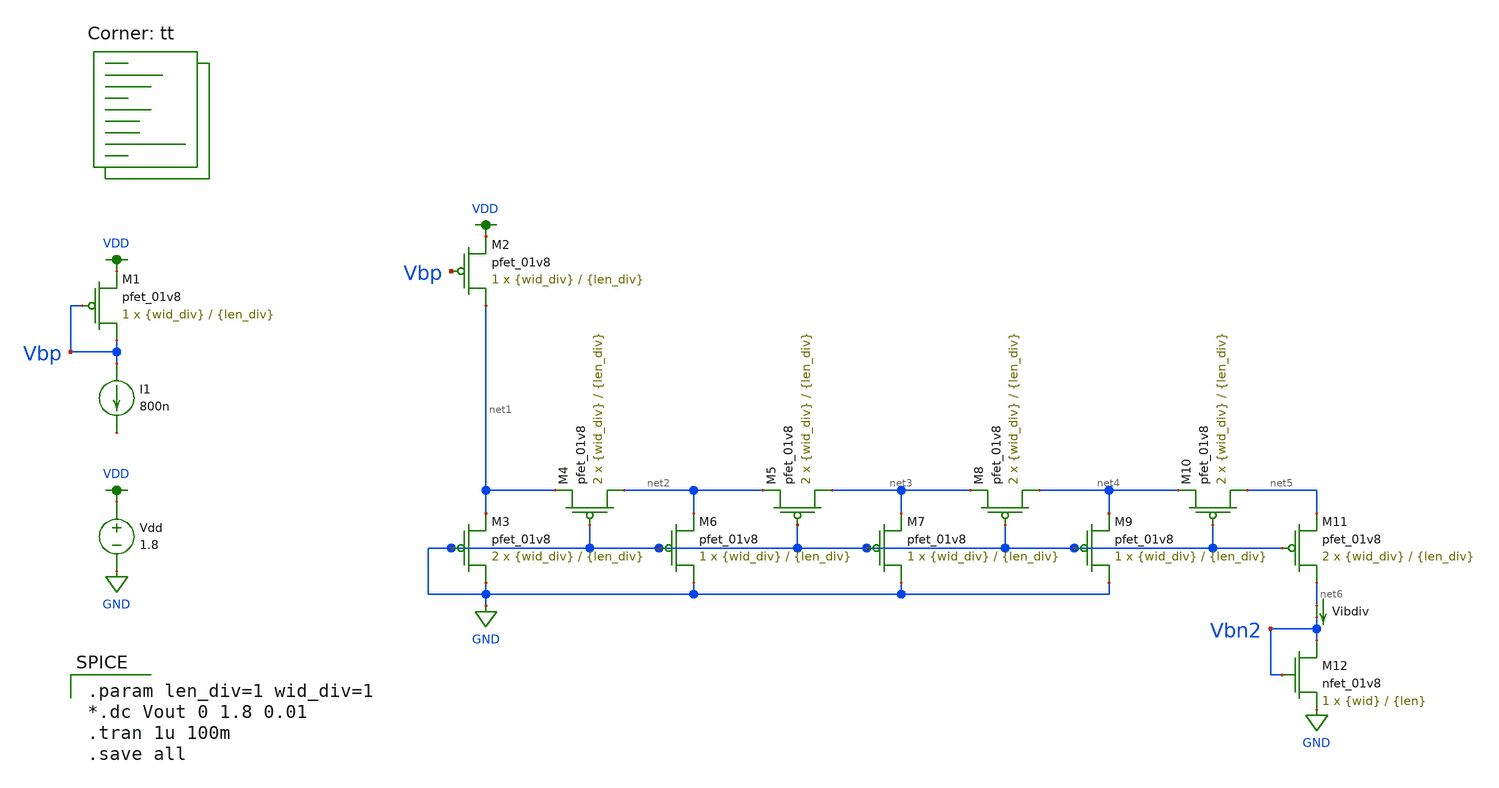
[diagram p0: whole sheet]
** sch_path: mp3/Reference Designs/current_divider_tb.sch
**.subckt current_divider_tb
I1 Vbp net7 800n
Vdd VDD GND 1.8
XM1 Vbp Vbp VDD VDD sky130_fd_pr__pfet_01v8 L={len_div} W={wid_div} nf=1 ad='int((nf+1)/2) * W/nf * 0.29'
+ as='int((nf+2)/2) * W/nf * 0.29' pd='2*int((nf+1)/2) * (W/nf + 0.29)' ps='2*int((nf+2)/2) * (W/nf + 0.29)'
+ nrd='0.29 / W' nrs='0.29 / W' sa=0 sb=0 sd=0 mult=1 m=1
XM2 net1 Vbp VDD VDD sky130_fd_pr__pfet_01v8 L={len_div} W={wid_div} nf=1 ad='int((nf+1)/2) * W/nf * 0.29'
+ as='int((nf+2)/2) * W/nf * 0.29' pd='2*int((nf+1)/2) * (W/nf + 0.29)' ps='2*int((nf+2)/2) * (W/nf + 0.29)'
+ nrd='0.29 / W' nrs='0.29 / W' sa=0 sb=0 sd=0 mult=1 m=1
XM3 GND GND net1 VDD sky130_fd_pr__pfet_01v8 L={len_div} W={wid_div} nf=1 ad='int((nf+1)/2) * W/nf * 0.29'
+ as='int((nf+2)/2) * W/nf * 0.29' pd='2*int((nf+1)/2) * (W/nf + 0.29)' ps='2*int((nf+2)/2) * (W/nf + 0.29)'
+ nrd='0.29 / W' nrs='0.29 / W' sa=0 sb=0 sd=0 mult=2 m=2
XM4 net2 GND net1 VDD sky130_fd_pr__pfet_01v8 L={len_div} W={wid_div} nf=1 ad='int((nf+1)/2) * W/nf * 0.29'
+ as='int((nf+2)/2) * W/nf * 0.29' pd='2*int((nf+1)/2) * (W/nf + 0.29)' ps='2*int((nf+2)/2) * (W/nf + 0.29)'
+ nrd='0.29 / W' nrs='0.29 / W' sa=0 sb=0 sd=0 mult=2 m=2
XM6 GND GND net2 VDD sky130_fd_pr__pfet_01v8 L={len_div} W={wid_div} nf=1 ad='int((nf+1)/2) * W/nf * 0.29'
+ as='int((nf+2)/2) * W/nf * 0.29' pd='2*int((nf+1)/2) * (W/nf + 0.29)' ps='2*int((nf+2)/2) * (W/nf + 0.29)'
+ nrd='0.29 / W' nrs='0.29 / W' sa=0 sb=0 sd=0 mult=1 m=1
XM5 net3 GND net2 VDD sky130_fd_pr__pfet_01v8 L={len_div} W={wid_div} nf=1 ad='int((nf+1)/2) * W/nf * 0.29'
+ as='int((nf+2)/2) * W/nf * 0.29' pd='2*int((nf+1)/2) * (W/nf + 0.29)' ps='2*int((nf+2)/2) * (W/nf + 0.29)'
+ nrd='0.29 / W' nrs='0.29 / W' sa=0 sb=0 sd=0 mult=2 m=2
XM7 GND GND net3 VDD sky130_fd_pr__pfet_01v8 L={len_div} W={wid_div} nf=1 ad='int((nf+1)/2) * W/nf * 0.29'
+ as='int((nf+2)/2) * W/nf * 0.29' pd='2*int((nf+1)/2) * (W/nf + 0.29)' ps='2*int((nf+2)/2) * (W/nf + 0.29)'
+ nrd='0.29 / W' nrs='0.29 / W' sa=0 sb=0 sd=0 mult=1 m=1
XM8 net4 GND net3 VDD sky130_fd_pr__pfet_01v8 L={len_div} W={wid_div} nf=1 ad='int((nf+1)/2) * W/nf * 0.29'
+ as='int((nf+2)/2) * W/nf * 0.29' pd='2*int((nf+1)/2) * (W/nf + 0.29)' ps='2*int((nf+2)/2) * (W/nf + 0.29)'
+ nrd='0.29 / W' nrs='0.29 / W' sa=0 sb=0 sd=0 mult=2 m=2
XM9 GND GND net4 VDD sky130_fd_pr__pfet_01v8 L={len_div} W={wid_div} nf=1 ad='int((nf+1)/2) * W/nf * 0.29'
+ as='int((nf+2)/2) * W/nf * 0.29' pd='2*int((nf+1)/2) * (W/nf + 0.29)' ps='2*int((nf+2)/2) * (W/nf + 0.29)'
+ nrd='0.29 / W' nrs='0.29 / W' sa=0 sb=0 sd=0 mult=1 m=1
XM10 net5 GND net4 VDD sky130_fd_pr__pfet_01v8 L={len_div} W={wid_div} nf=1 ad='int((nf+1)/2) * W/nf * 0.29'
+ as='int((nf+2)/2) * W/nf * 0.29' pd='2*int((nf+1)/2) * (W/nf + 0.29)' ps='2*int((nf+2)/2) * (W/nf + 0.29)'
+ nrd='0.29 / W' nrs='0.29 / W' sa=0 sb=0 sd=0 mult=2 m=2
XM11 net6 GND net5 VDD sky130_fd_pr__pfet_01v8 L={len_div} W={wid_div} nf=1 ad='int((nf+1)/2) * W/nf * 0.29'
+ as='int((nf+2)/2) * W/nf * 0.29' pd='2*int((nf+1)/2) * (W/nf + 0.29)' ps='2*int((nf+2)/2) * (W/nf + 0.29)'
+ nrd='0.29 / W' nrs='0.29 / W' sa=0 sb=0 sd=0 mult=2 m=2
XM12 Vbn2 Vbn2 GND GND sky130_fd_pr__nfet_01v8 L={len} W={wid} nf=1 ad='int((nf+1)/2) * W/nf * 0.29'
+ as='int((nf+2)/2) * W/nf * 0.29' pd='2*int((nf+1)/2) * (W/nf + 0.29)' ps='2*int((nf+2)/2) * (W/nf + 0.29)'
+ nrd='0.29 / W' nrs='0.29 / W' sa=0 sb=0 sd=0 mult=1 m=1
Vibdiv net6 Vbn2 0
.save i(vibdiv)
**** begin user architecture code
.lib $::SKYWATER_MODELS/sky130.lib.spice tt

.param len_div=1 wid_div=1
*.dc Vout 0 1.8 0.01
.tran 1u 100m
.save all


**** end user architecture code
**.ends
.GLOBAL VDD
.GLOBAL GND
.end
